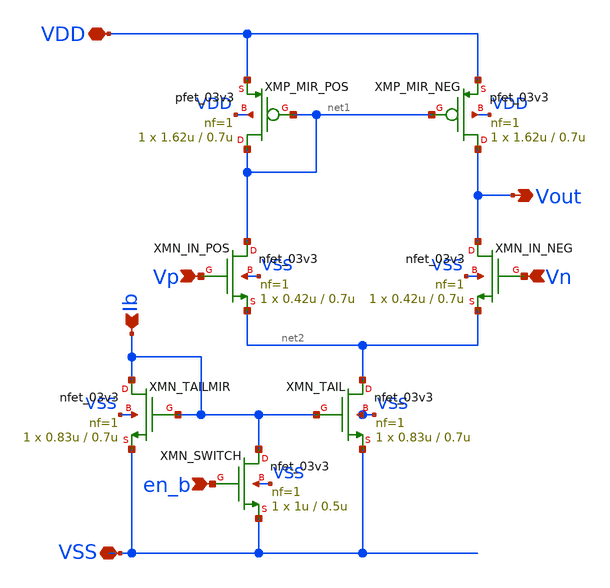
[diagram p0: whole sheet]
** sch_path: Analog/schematics/1_readout/bpf/B18_BPF_OTA.sch
**.subckt B18_BPF_OTA Vp Vn Vout VDD VSS Ib en_b
*.ipin Vp
*.ipin Vn
*.opin Vout
*.iopin VDD
*.iopin VSS
*.ipin Ib
*.ipin en_b
XMP_MIR_NEG Vout net1 VDD VDD pfet_03v3 L=0.7u W=1.62u nf=1 ad='int((nf+1)/2) * W/nf * 0.18u' as='int((nf+2)/2) * W/nf * 0.18u'
+ pd='2*int((nf+1)/2) * (W/nf + 0.18u)' ps='2*int((nf+2)/2) * (W/nf + 0.18u)' nrd='0.18u / W' nrs='0.18u / W'
+ sa=0 sb=0 sd=0 m=1
XMP_MIR_POS net1 net1 VDD VDD pfet_03v3 L=0.7u W=1.62u nf=1 ad='int((nf+1)/2) * W/nf * 0.18u' as='int((nf+2)/2) * W/nf * 0.18u'
+ pd='2*int((nf+1)/2) * (W/nf + 0.18u)' ps='2*int((nf+2)/2) * (W/nf + 0.18u)' nrd='0.18u / W' nrs='0.18u / W'
+ sa=0 sb=0 sd=0 m=1
XMN_IN_POS net1 Vp net2 VSS nfet_03v3 L=0.7u W=0.42u nf=1 ad='int((nf+1)/2) * W/nf * 0.18u' as='int((nf+2)/2) * W/nf * 0.18u'
+ pd='2*int((nf+1)/2) * (W/nf + 0.18u)' ps='2*int((nf+2)/2) * (W/nf + 0.18u)' nrd='0.18u / W' nrs='0.18u / W'
+ sa=0 sb=0 sd=0 m=1
XMN_IN_NEG Vout Vn net2 VSS nfet_03v3 L=0.7u W=0.42u nf=1 ad='int((nf+1)/2) * W/nf * 0.18u' as='int((nf+2)/2) * W/nf * 0.18u'
+ pd='2*int((nf+1)/2) * (W/nf + 0.18u)' ps='2*int((nf+2)/2) * (W/nf + 0.18u)' nrd='0.18u / W' nrs='0.18u / W'
+ sa=0 sb=0 sd=0 m=1
XMN_TAIL net2 Ib VSS VSS nfet_03v3 L=0.7u W=0.83u nf=1 ad='int((nf+1)/2) * W/nf * 0.18u' as='int((nf+2)/2) * W/nf * 0.18u'
+ pd='2*int((nf+1)/2) * (W/nf + 0.18u)' ps='2*int((nf+2)/2) * (W/nf + 0.18u)' nrd='0.18u / W' nrs='0.18u / W'
+ sa=0 sb=0 sd=0 m=1
XMN_TAILMIR Ib Ib VSS VSS nfet_03v3 L=0.7u W=0.83u nf=1 ad='int((nf+1)/2) * W/nf * 0.18u' as='int((nf+2)/2) * W/nf * 0.18u'
+ pd='2*int((nf+1)/2) * (W/nf + 0.18u)' ps='2*int((nf+2)/2) * (W/nf + 0.18u)' nrd='0.18u / W' nrs='0.18u / W'
+ sa=0 sb=0 sd=0 m=1
XMN_SWITCH Ib en_b VSS VSS nfet_03v3 L=0.5u W=1u nf=1 ad='int((nf+1)/2) * W/nf * 0.18u' as='int((nf+2)/2) * W/nf * 0.18u'
+ pd='2*int((nf+1)/2) * (W/nf + 0.18u)' ps='2*int((nf+2)/2) * (W/nf + 0.18u)' nrd='0.18u / W' nrs='0.18u / W'
+ sa=0 sb=0 sd=0 m=1
**.ends
.end
